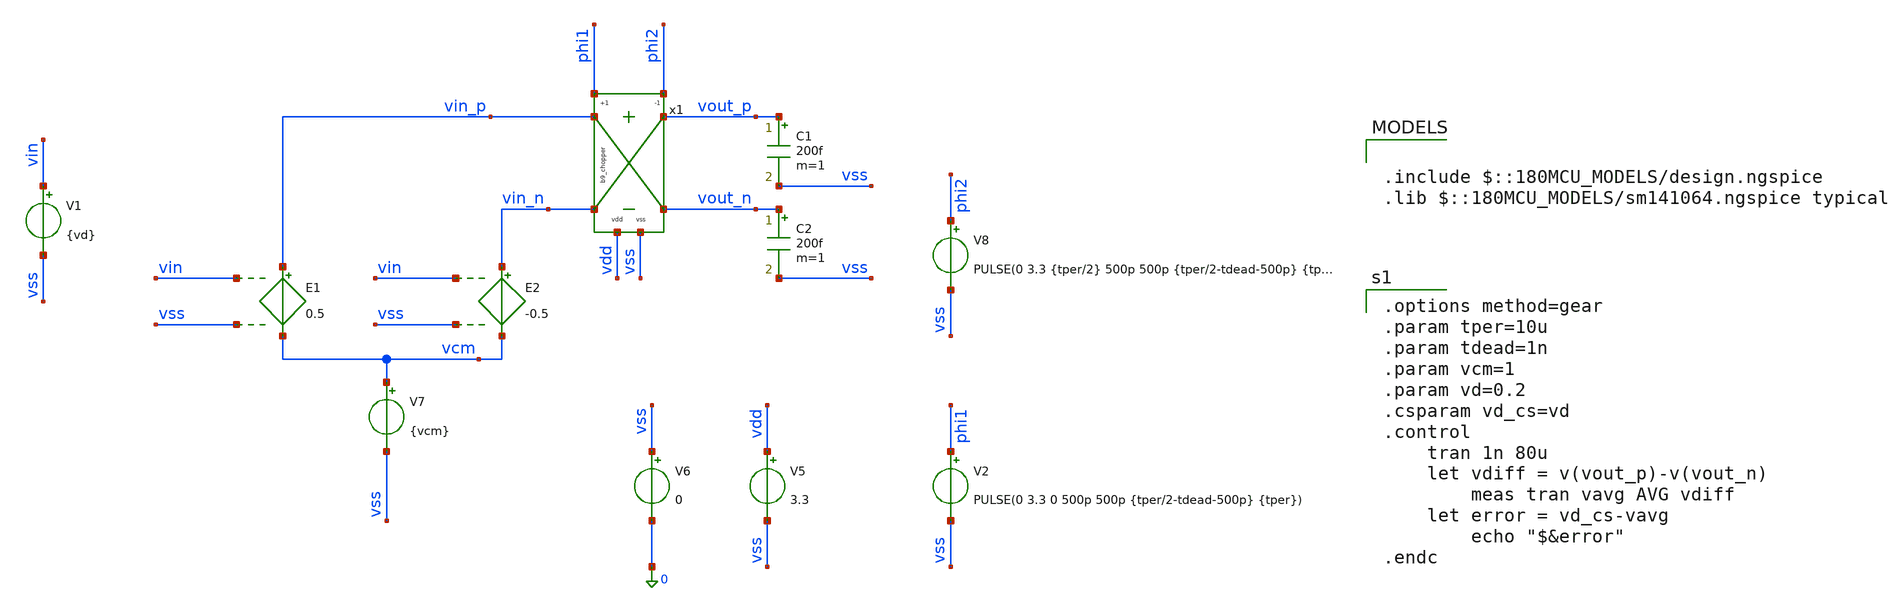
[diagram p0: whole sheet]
** sch_path: xschem/chopper/b9_chopper_tb_basic.sch
**.subckt b9_chopper_tb_basic
x1 vdd phi1 vss vin_p phi2 vin_n vout_p vout_n b9_chopper
V7 vcm vss {vcm}
E1 vin_p vcm vin vss 0.5
E2 vin_n vcm vin vss -0.5
C1 vout_p vss 200f m=1
C2 vout_n vss 200f m=1
V5 vdd vss 3.3
V6 vss 0 0
V1 vin vss {vd}
V2 phi1 vss PULSE(0 3.3 0 500p 500p {tper/2-tdead-500p} {tper})
V8 phi2 vss PULSE(0 3.3 {tper/2} 500p 500p {tper/2-tdead-500p} {tper})
**** begin user architecture code

.include $::180MCU_MODELS/design.ngspice
.lib $::180MCU_MODELS/sm141064.ngspice typical


.options method=gear
.param tper=10u
.param tdead=1n
.param vcm=1
.param vd=0.2
.csparam vd_cs=vd
.control
	tran 1n 80u
	let vdiff = v(vout_p)-v(vout_n)
        meas tran vavg AVG vdiff
	let error = vd_cs-vavg
        echo "$&error"
.endc

**** end user architecture code
**.ends

* expanding   symbol:  xschem/chopper/b9_chopper.sym # of pins=8
** sym_path: xschem/chopper/b9_chopper.sym
** sch_path: xschem/chopper/b9_chopper.sch
.subckt b9_chopper vdd phi1 vss vin_p phi2 vin_n vout_p vout_n
*.iopin vss
*.iopin vin_p
*.iopin vin_n
*.iopin vout_p
*.iopin vout_n
*.ipin phi1
*.ipin phi2
*.iopin vdd
x1 vdd vin_n vss vout_n phi1 b9_sw_chop
x2 vdd vin_n vss vout_p phi2 b9_sw_chop
x3 vdd vin_p vss vout_n phi2 b9_sw_chop
x4 vdd vin_p vss vout_p phi1 b9_sw_chop
.ends


* expanding   symbol:  xschem/sw/b9_sw_chop.sym # of pins=5
** sym_path: xschem/sw/b9_sw_chop.sym
** sch_path: xschem/sw/b9_sw_chop.sch
.subckt b9_sw_chop vdd va vss vb en
*.iopin vdd
*.iopin vss
*.iopin en
*.iopin va
*.iopin vb
XM1 vb en va vss nfet_03v3 L=0.28u W=9.6u nf=4 ad='int((nf+1)/2) * W/nf * 0.18u' as='int((nf+2)/2) * W/nf * 0.18u'
+ pd='2*int((nf+1)/2) * (W/nf + 0.18u)' ps='2*int((nf+2)/2) * (W/nf + 0.18u)' nrd='0.18u / W' nrs='0.18u / W'
+ sa=0 sb=0 sd=0 m=1
.ends

.end
